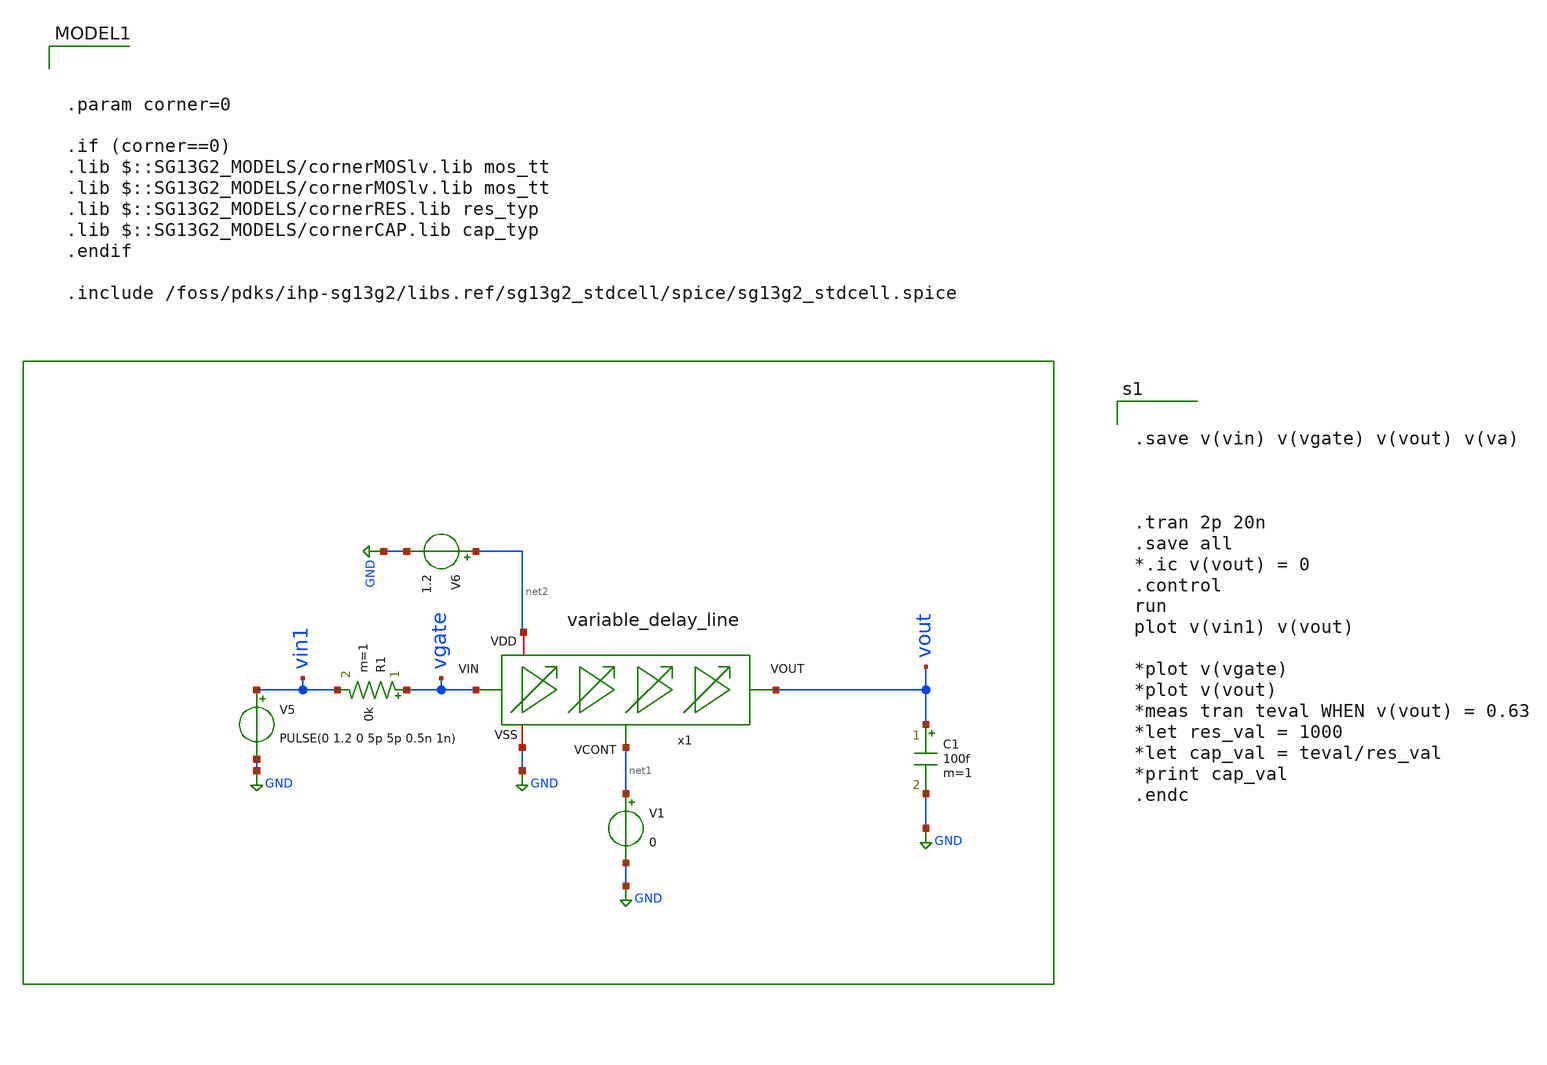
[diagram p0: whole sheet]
** sch_path: sch/delay_variable_line/tb_variable_delay_line.sch
**.subckt tb_variable_delay_line
x1 net3 GND net1 vout vgate variable_delay_line
C1 vout GND 100f m=1
V1 net1 GND 0
R1 vgate vin1 0k m=1
V5 vin1 GND PULSE(0 1.2 0 5p 5p 0.5n 1n)
V6 net2 GND 1.2
**** begin user architecture code


.save v(vin) v(vgate) v(vout) v(va)



.tran 2p 20n
.save all
*.ic v(vout) = 0
.control
run
plot v(vin1) v(vout)

*plot v(vgate)
*plot v(vout)
*meas tran teval WHEN v(vout) = 0.63
*let res_val = 1000
*let cap_val = teval/res_val
*print cap_val
.endc




.param corner=0

.if (corner==0)
.lib $::SG13G2_MODELS/cornerMOSlv.lib mos_tt
.lib $::SG13G2_MODELS/cornerMOSlv.lib mos_tt
.lib $::SG13G2_MODELS/cornerRES.lib res_typ
.lib $::SG13G2_MODELS/cornerCAP.lib cap_typ
.endif

.include /foss/pdks/ihp-sg13g2/libs.ref/sg13g2_stdcell/spice/sg13g2_stdcell.spice

**** end user architecture code
**.ends

* expanding   symbol:  /foss/designs/UNIC-CASS-Aug25/sch/delay_variable_line/variable_delay_line.sym
*+ # of pins=5
** sym_path: sch/delay_variable_line/variable_delay_line.sym
** sch_path: sch/delay_variable_line/variable_delay_line.sch
.subckt variable_delay_line VDD VSS VCONT VOUT VIN
*.iopin VSS
*.iopin VDD
*.ipin VIN
*.opin VOUT
*.ipin VCONT
x1 VDD VIN net1 VCONT VSS variable_delay
x2 VDD net1 net2 VCONT VSS variable_delay
x3 VDD net2 net5 VCONT VSS variable_delay
x4 VDD net5 net3 VCONT VSS variable_delay
x5 VDD net3 net4 VCONT VSS variable_delay
x6 VDD net4 VOUT VCONT VSS variable_delay
.ends


* expanding   symbol:  /foss/designs/DLL/variable_delay.sym # of pins=5
** sym_path: sch/delay_variable_line/variable_delay.sym
** sch_path: sch/delay_variable_line/variable_delay.sch
.subckt variable_delay VDD_D VIN_D VOUT_D VCONT_D VSS_D
*.iopin VSS_D
*.iopin VDD_D
*.ipin VIN_D
*.opin VOUT_D
*.ipin VCONT_D
XM3 net4 VCONT_D net2 net2 sg13_lv_nmos w=1u l=0.13u ng=1 m=1 mm_ok=1
XM5 net3 VCONT_D net2 net2 sg13_lv_nmos w=1u l=5u ng=1 m=1 mm_ok=1
XM4 net4 net4 VDD_D VDD_D sg13_lv_pmos w=1u l=0.13u ng=1 m=1 mm_ok=1
XM6 net1 net4 VDD_D VDD_D sg13_lv_pmos w=1u l=5u ng=1 m=1 mm_ok=1
XM2 VOUT_D VIN_D net1 VDD_D sg13_lv_pmos w=10u l=10u ng=1 m=1 mm_ok=1
XM1 VOUT_D VIN_D net3 net2 sg13_lv_nmos w=10u l=10u ng=1 m=1 mm_ok=1
.ends

.GLOBAL GND
.end
